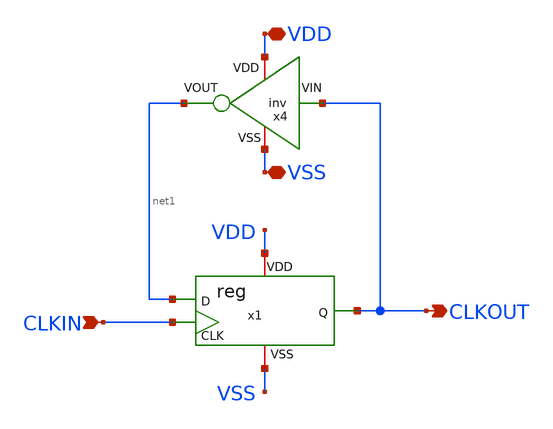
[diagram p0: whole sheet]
** sch_path: Custom_std_cells/div_freq_x2.sch
**.subckt div_freq_x2 VDD VSS CLKIN CLKOUT
*.iopin VDD
*.iopin VSS
*.ipin CLKIN
*.opin CLKOUT
x1 VDD CLKIN CLKOUT net1 VSS reg
x4 VDD net1 CLKOUT VSS inv
**.ends

* expanding   symbol:  /foss/designs/PhaseInterpolator/Custom_std_Cells/reg.sym # of pins=5
** sym_path: /foss/designs/PhaseInterpolator/Custom_std_Cells/reg.sym
** sch_path: /foss/designs/PhaseInterpolator/Custom_std_Cells/reg.sch
.subckt reg VDD CLK Q D VSS
*.ipin D
*.opin Q
*.iopin VDD
*.iopin VSS
*.ipin CLK
XM2 X CLK net1 VDD sg13_lv_pmos w=0.15u l=0.13u ng=1 m=1 mm_ok=1
XM1 X CLK_B net2 VSS sg13_lv_nmos w=0.15u l=0.13u ng=1 m=1 mm_ok=1
XM3 net1 D VDD VDD sg13_lv_pmos w=0.15u l=0.13u ng=1 m=1 mm_ok=1
XM4 net2 D VSS VSS sg13_lv_nmos w=0.15u l=0.13u ng=1 m=1 mm_ok=1
XM5 Q CLK_B net3 VDD sg13_lv_pmos w=0.15u l=0.13u ng=1 m=1 mm_ok=1
XM6 Q CLK net4 VSS sg13_lv_nmos w=0.15u l=0.13u ng=1 m=1 mm_ok=1
XM7 net3 X VDD VDD sg13_lv_pmos w=0.15u l=0.13u ng=1 m=1 mm_ok=1
XM8 net4 X VSS VSS sg13_lv_nmos w=0.15u l=0.13u ng=1 m=1 mm_ok=1
x1 VDD CLK_B CLK VSS inv
.ends

.end
